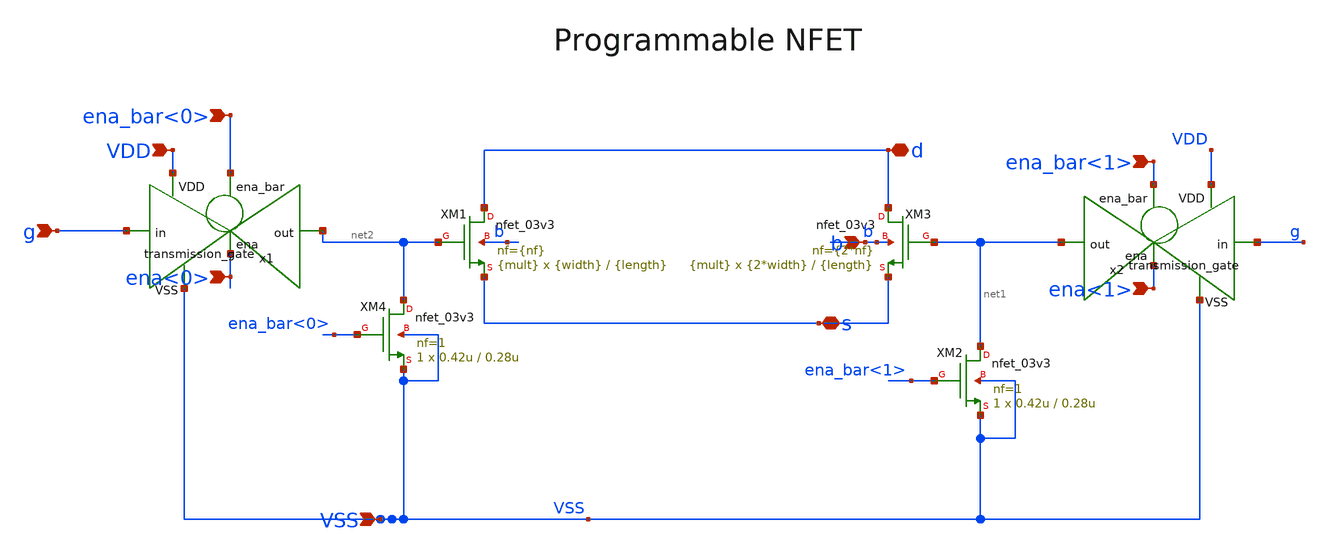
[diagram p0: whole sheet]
** sch_path: designs/libs/core_digital/schem/programmable_nfet.sch
**.subckt programmable_nfet VSS VDD g ena_bar<1> ena_bar<0> ena<1> ena<0> d s b
*.ipin VSS
*.ipin VDD
*.ipin g
*.ipin ena_bar<1>
*.ipin ena_bar<0>
*.ipin ena<1>
*.ipin ena<0>
*.iopin d
*.iopin s
*.ipin b
XM1 d net2 s b nfet_03v3 L={length} W={width} nf={nf} ad='int((nf+1)/2) * W/nf * 0.18u' as='int((nf+2)/2) * W/nf * 0.18u'
+ pd='2*int((nf+1)/2) * (W/nf + 0.18u)' ps='2*int((nf+2)/2) * (W/nf + 0.18u)' nrd='0.18u / W' nrs='0.18u / W'
+ sa=0 sb=0 sd=0 m={mult}
XM3 d net1 s b nfet_03v3 L={length} W={2*width} nf={2*nf} ad='int((nf+1)/2) * W/nf * 0.18u' as='int((nf+2)/2) * W/nf * 0.18u'
+ pd='2*int((nf+1)/2) * (W/nf + 0.18u)' ps='2*int((nf+2)/2) * (W/nf + 0.18u)' nrd='0.18u / W' nrs='0.18u / W'
+ sa=0 sb=0 sd=0 m={mult}
XM2 net1 ena_bar<1> VSS VSS nfet_03v3 L=0.28u W=0.42u nf=1 ad='int((nf+1)/2) * W/nf * 0.18u' as='int((nf+2)/2) * W/nf * 0.18u'
+ pd='2*int((nf+1)/2) * (W/nf + 0.18u)' ps='2*int((nf+2)/2) * (W/nf + 0.18u)' nrd='0.18u / W' nrs='0.18u / W'
+ sa=0 sb=0 sd=0 m=1
XM4 net2 ena_bar<0> VSS VSS nfet_03v3 L=0.28u W=0.42u nf=1 ad='int((nf+1)/2) * W/nf * 0.18u' as='int((nf+2)/2) * W/nf * 0.18u'
+ pd='2*int((nf+1)/2) * (W/nf + 0.18u)' ps='2*int((nf+2)/2) * (W/nf + 0.18u)' nrd='0.18u / W' nrs='0.18u / W'
+ sa=0 sb=0 sd=0 m=1
x1 ena_bar<0> VDD net2 g VSS ena<0> transmission_gate
x2 ena_bar<1> VDD net1 g VSS ena<1> transmission_gate
**.ends

* expanding   symbol:  libs/core_digital/schem/transmission_gate.sym # of pins=6
** sym_path: designs/libs/core_digital/schem/transmission_gate.sym
** sch_path: designs/libs/core_digital/schem/transmission_gate.sch
.subckt transmission_gate ena_bar VDD out in VSS ena
*.ipin in
*.ipin ena_bar
*.ipin ena
*.ipin VSS
*.ipin VDD
*.opin out
XM1 in ena_bar out VDD pfet_03v3 L=0.28u W=0.42u nf=1 ad='int((nf+1)/2) * W/nf * 0.18u' as='int((nf+2)/2) * W/nf * 0.18u'
+ pd='2*int((nf+1)/2) * (W/nf + 0.18u)' ps='2*int((nf+2)/2) * (W/nf + 0.18u)' nrd='0.18u / W' nrs='0.18u / W'
+ sa=0 sb=0 sd=0 m=1
XM2 in ena out VSS nfet_03v3 L=0.28u W=0.42u nf=1 ad='int((nf+1)/2) * W/nf * 0.18u' as='int((nf+2)/2) * W/nf * 0.18u'
+ pd='2*int((nf+1)/2) * (W/nf + 0.18u)' ps='2*int((nf+2)/2) * (W/nf + 0.18u)' nrd='0.18u / W' nrs='0.18u / W'
+ sa=0 sb=0 sd=0 m=1
.ends

.end
